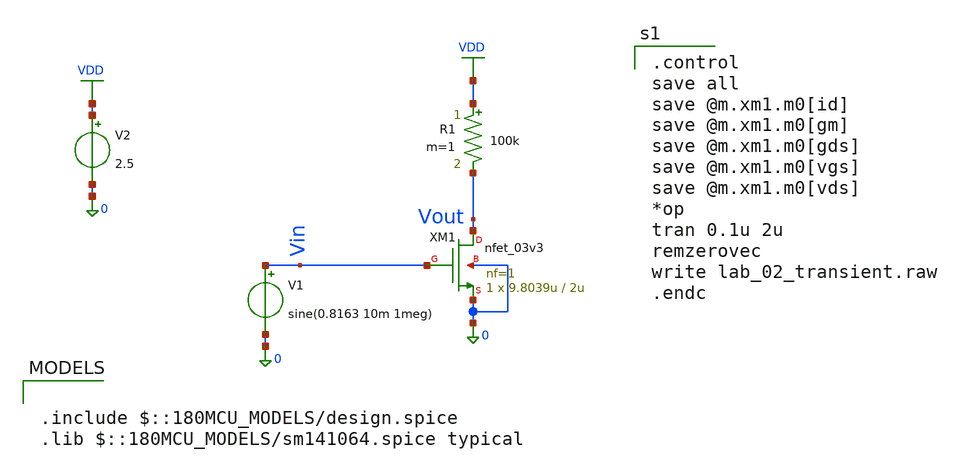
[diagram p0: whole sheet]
** sch_path: Lab_02/Lab_02_trans.sch
**.subckt Lab_02_trans
XM1 Vout Vin 0 0 nfet_03v3 L=2u W=9.8039u nf=1 ad='int((nf+1)/2) * W/nf * 0.18u' as='int((nf+2)/2) * W/nf * 0.18u'
+ pd='2*int((nf+1)/2) * (W/nf + 0.18u)' ps='2*int((nf+2)/2) * (W/nf + 0.18u)' nrd='0.18u / W' nrs='0.18u / W'
+ sa=0 sb=0 sd=0 m=1
R1 VDD Vout 100k m=1
V1 Vin 0 sine(0.8163 10m 1meg)
V2 VDD 0 2.5
**** begin user architecture code

.include $::180MCU_MODELS/design.spice
.lib $::180MCU_MODELS/sm141064.spice typical


.control
save all
save @m.xm1.m0[id]
save @m.xm1.m0[gm]
save @m.xm1.m0[gds]
save @m.xm1.m0[vgs]
save @m.xm1.m0[vds]
*op
tran 0.1u 2u
remzerovec
write lab_02_transient.raw
.endc

**** end user architecture code
**.ends
.GLOBAL VDD
.end
